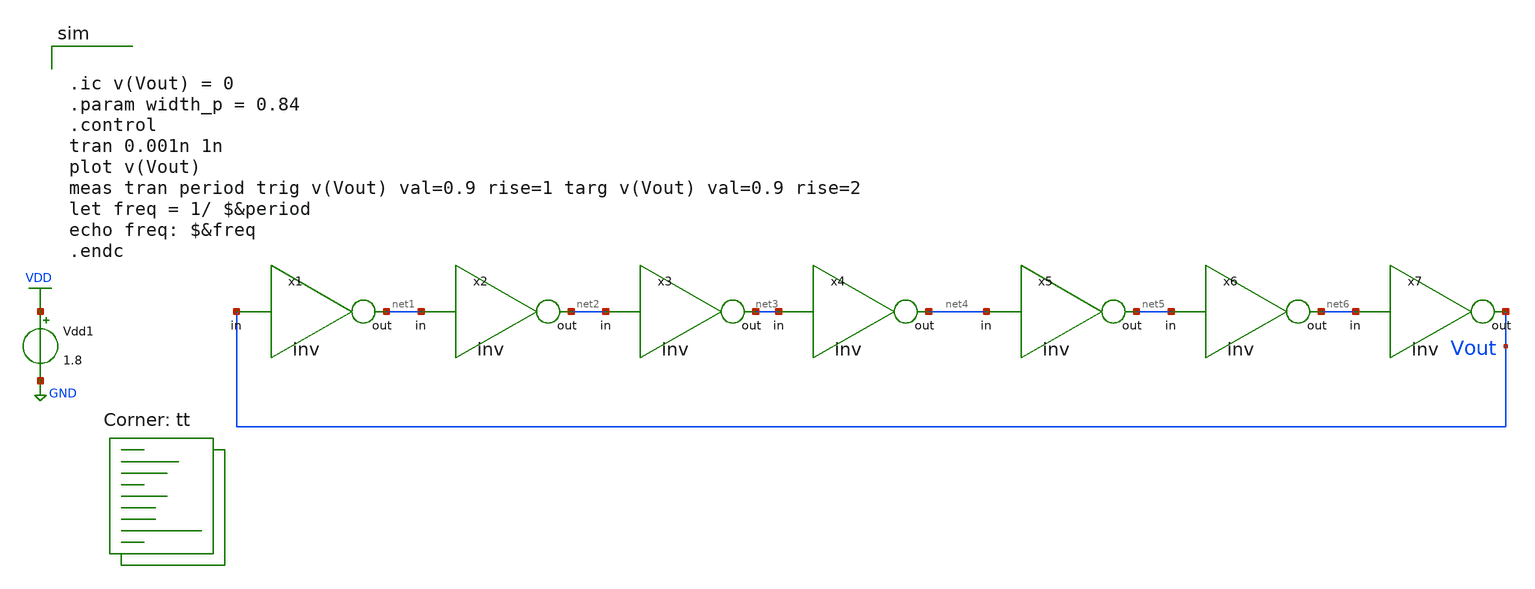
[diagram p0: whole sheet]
** sch_path: tutorial_4/tutorial_4_2a.sch
**.subckt tutorial_4_2a
x1 net1 Vout inv
x2 net2 net1 inv
x3 net3 net2 inv
x4 net4 net3 inv
x5 net5 net4 inv
x6 net6 net5 inv
x7 Vout net6 inv
Vdd1 VDD GND 1.8
**** begin user architecture code


.ic v(Vout) = 0
.param width_p = 0.84
.control
tran 0.001n 1n
plot v(Vout)
meas tran period trig v(Vout) val=0.9 rise=1 targ v(Vout) val=0.9 rise=2
let freq = 1/ $&period
echo freq: $&freq
.endc

.lib $::SKYWATER_MODELS/sky130.lib.spice tt
**** end user architecture code
**.ends

* expanding   symbol:  /home/EE23B038/ee5311/tutorial_4/inv.sym # of pins=2
** sym_path: tutorial_4/inv.sym
** sch_path: tutorial_4/inv.sch
.subckt inv out in
*.ipin in
*.opin out
XM1 out in GND GND sky130_fd_pr__nfet_01v8 L=0.15 W=0.42 nf=1 ad='int((nf+1)/2) * W/nf * 0.29' as='int((nf+2)/2) * W/nf * 0.29'
+ pd='2*int((nf+1)/2) * (W/nf + 0.29)' ps='2*int((nf+2)/2) * (W/nf + 0.29)' nrd='0.29 / W' nrs='0.29 / W'
+ sa=0 sb=0 sd=0 mult=1 m=1
XM2 out in VDD VDD sky130_fd_pr__pfet_01v8 L=0.15 W={width_p} nf=1 ad='int((nf+1)/2) * W/nf * 0.29' as='int((nf+2)/2) * W/nf * 0.29'
+ pd='2*int((nf+1)/2) * (W/nf + 0.29)' ps='2*int((nf+2)/2) * (W/nf + 0.29)' nrd='0.29 / W' nrs='0.29 / W'
+ sa=0 sb=0 sd=0 mult=1 m=1
.ends

.GLOBAL GND
.GLOBAL VDD
.end
